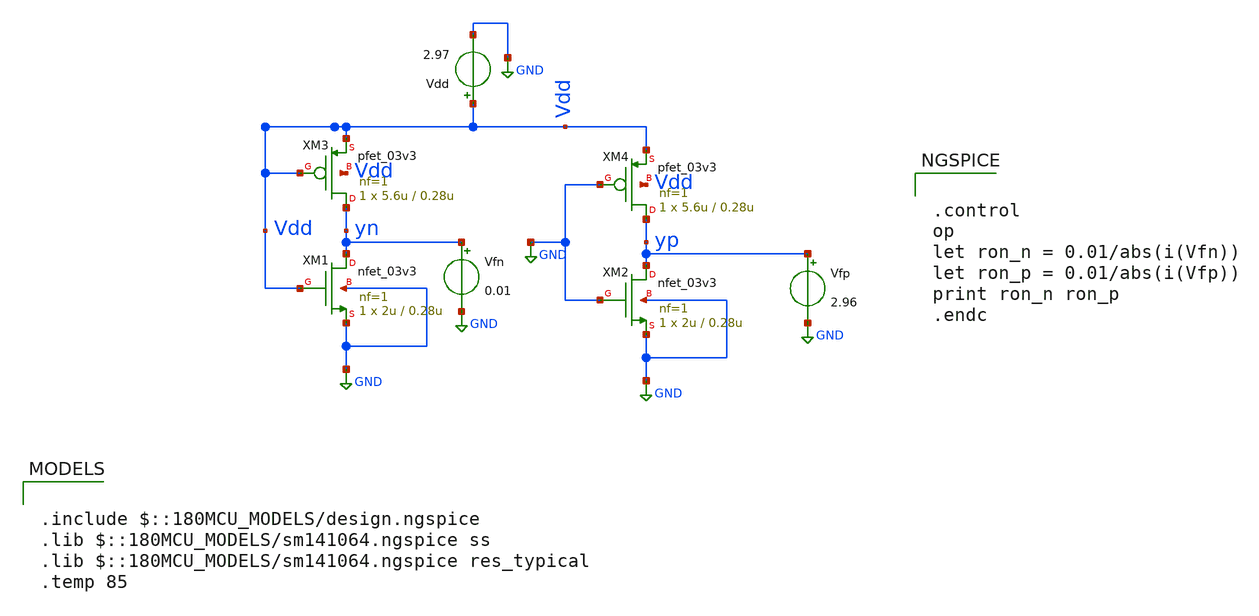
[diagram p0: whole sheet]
** sch_path: xschem/pll_dac/switch_ron.sch
**.subckt switch_ron
XM1 yn Vdd GND GND nfet_03v3 L=0.28u W=2u nf=1 ad='int((nf+1)/2) * W/nf * 0.18u' as='int((nf+2)/2) * W/nf * 0.18u'
+ pd='2*int((nf+1)/2) * (W/nf + 0.18u)' ps='2*int((nf+2)/2) * (W/nf + 0.18u)' nrd='0.18u / W' nrs='0.18u / W'
+ sa=0 sb=0 sd=0 m=1
XM3 yn Vdd Vdd Vdd pfet_03v3 L=0.28u W=5.6u nf=1 ad='int((nf+1)/2) * W/nf * 0.18u' as='int((nf+2)/2) * W/nf * 0.18u'
+ pd='2*int((nf+1)/2) * (W/nf + 0.18u)' ps='2*int((nf+2)/2) * (W/nf + 0.18u)' nrd='0.18u / W' nrs='0.18u / W'
+ sa=0 sb=0 sd=0 m=1
XM2 yp GND GND GND nfet_03v3 L=0.28u W=2u nf=1 ad='int((nf+1)/2) * W/nf * 0.18u' as='int((nf+2)/2) * W/nf * 0.18u'
+ pd='2*int((nf+1)/2) * (W/nf + 0.18u)' ps='2*int((nf+2)/2) * (W/nf + 0.18u)' nrd='0.18u / W' nrs='0.18u / W'
+ sa=0 sb=0 sd=0 m=1
XM4 yp GND Vdd Vdd pfet_03v3 L=0.28u W=5.6u nf=1 ad='int((nf+1)/2) * W/nf * 0.18u' as='int((nf+2)/2) * W/nf * 0.18u'
+ pd='2*int((nf+1)/2) * (W/nf + 0.18u)' ps='2*int((nf+2)/2) * (W/nf + 0.18u)' nrd='0.18u / W' nrs='0.18u / W'
+ sa=0 sb=0 sd=0 m=1
Vdd Vdd GND 2.97
Vfn yn GND 0.01
Vfp yp GND 2.96
**** begin user architecture code

.include $::180MCU_MODELS/design.ngspice
.lib $::180MCU_MODELS/sm141064.ngspice ss
.lib $::180MCU_MODELS/sm141064.ngspice res_typical
.temp 85



.control
op
let ron_n = 0.01/abs(i(Vfn))
let ron_p = 0.01/abs(i(Vfp))
print ron_n ron_p
.endc


**** end user architecture code
**.ends
.GLOBAL GND
.end
